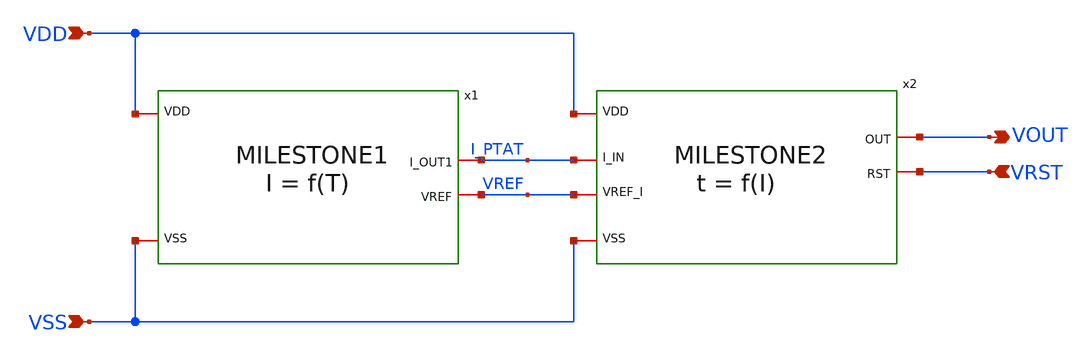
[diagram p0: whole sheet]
** sch_path: design/CNR_GR03_SKY130NM/TOPLEVEL.sch
**.subckt TOPLEVEL VDD VSS VOUT VRST
*.ipin VDD
*.ipin VSS
*.opin VOUT
*.ipin VRST
x1 VDD I_PTAT VREF VSS MILESTONE1
x2 I_PTAT VREF VOUT VDD VRST VSS MILESTONE2
**.ends
.end
